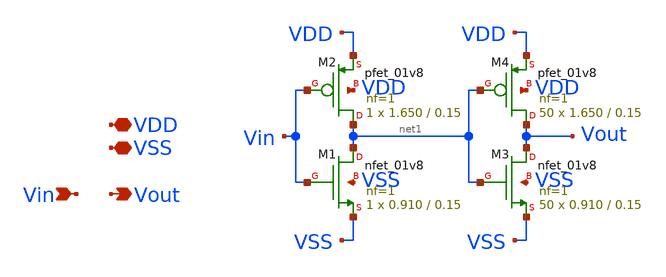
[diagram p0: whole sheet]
** sch_path: xschem/src/capacitor_switch/capacitor_switch.sch
**.subckt capacitor_switch VDD Vin Vout VSS
*.iopin VDD
*.ipin Vin
*.opin Vout
*.iopin VSS
XM1 net1 Vin VSS VSS sky130_fd_pr__nfet_01v8 L=0.15 W=0.910 nf=1 ad='int((nf+1)/2) * W/nf * 0.29' as='int((nf+2)/2) * W/nf * 0.29'
+ pd='2*int((nf+1)/2) * (W/nf + 0.29)' ps='2*int((nf+2)/2) * (W/nf + 0.29)' nrd='0.29 / W' nrs='0.29 / W'
+ sa=0 sb=0 sd=0 mult=1 m=1
XM2 net1 Vin VDD VDD sky130_fd_pr__pfet_01v8 L=0.15 W=1.650 nf=1 ad='int((nf+1)/2) * W/nf * 0.29' as='int((nf+2)/2) * W/nf * 0.29'
+ pd='2*int((nf+1)/2) * (W/nf + 0.29)' ps='2*int((nf+2)/2) * (W/nf + 0.29)' nrd='0.29 / W' nrs='0.29 / W'
+ sa=0 sb=0 sd=0 mult=1 m=1
XM3 Vout net1 VSS VSS sky130_fd_pr__nfet_01v8 L=0.15 W=0.910 nf=1 ad='int((nf+1)/2) * W/nf * 0.29' as='int((nf+2)/2) * W/nf * 0.29'
+ pd='2*int((nf+1)/2) * (W/nf + 0.29)' ps='2*int((nf+2)/2) * (W/nf + 0.29)' nrd='0.29 / W' nrs='0.29 / W'
+ sa=0 sb=0 sd=0 mult=50 m=50
XM4 Vout net1 VDD VDD sky130_fd_pr__pfet_01v8 L=0.15 W=1.650 nf=1 ad='int((nf+1)/2) * W/nf * 0.29' as='int((nf+2)/2) * W/nf * 0.29'
+ pd='2*int((nf+1)/2) * (W/nf + 0.29)' ps='2*int((nf+2)/2) * (W/nf + 0.29)' nrd='0.29 / W' nrs='0.29 / W'
+ sa=0 sb=0 sd=0 mult=50 m=50
**.ends
.end
